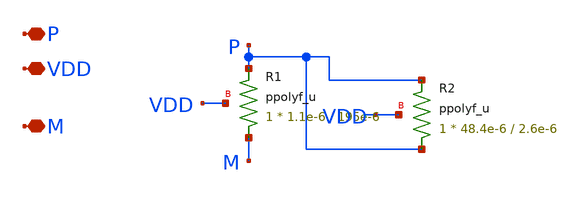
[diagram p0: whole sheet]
** sch_path: Clock_Generator_PAKISTAN_06/Xschem/Res_74k.sch
**.subckt Res_74k P VDD M
*.iopin P
*.iopin VDD
*.iopin M
XR1 M P VDD ppolyf_u r_width=1.1e-6 r_length=195e-6 m=1
XR2 P P VDD ppolyf_u r_width=48.4e-6 r_length=2.6e-6 m=1
**.ends
.end
